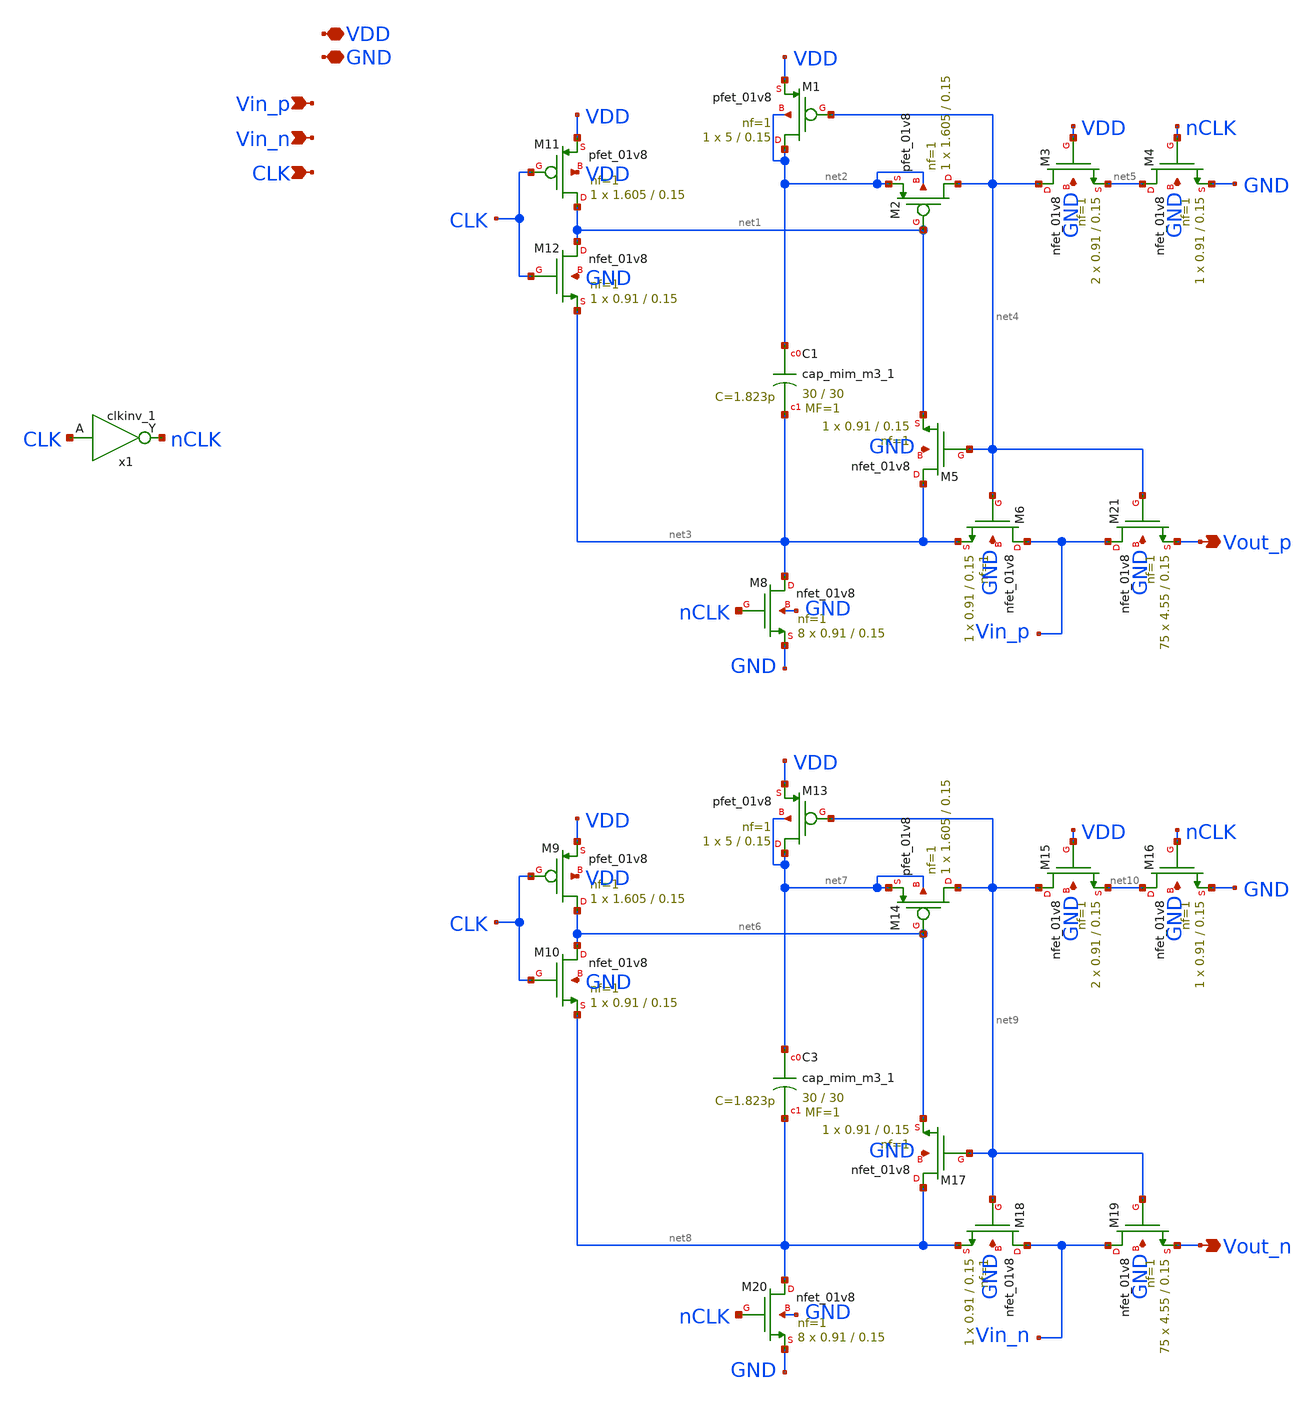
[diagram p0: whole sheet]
** sch_path: xschem/bootstrapped_switch/bsswitch.sch
**.subckt bsswitch Vin_p Vin_n CLK Vout_p Vout_n VDD GND
*.ipin Vin_p
*.ipin Vin_n
*.ipin CLK
*.opin Vout_p
*.opin Vout_n
*.iopin VDD
*.iopin GND
XM11 net1 CLK VDD VDD sky130_fd_pr__pfet_01v8 L=0.15 W=1.605 nf=1 ad='int((nf+1)/2) * W/nf * 0.29' as='int((nf+2)/2) * W/nf * 0.29'
+ pd='2*int((nf+1)/2) * (W/nf + 0.29)' ps='2*int((nf+2)/2) * (W/nf + 0.29)' nrd='0.29 / W' nrs='0.29 / W'
+ sa=0 sb=0 sd=0 mult=1 m=1
XM12 net1 CLK net3 GND sky130_fd_pr__nfet_01v8 L=0.15 W=0.91 nf=1 ad='int((nf+1)/2) * W/nf * 0.29' as='int((nf+2)/2) * W/nf * 0.29'
+ pd='2*int((nf+1)/2) * (W/nf + 0.29)' ps='2*int((nf+2)/2) * (W/nf + 0.29)' nrd='0.29 / W' nrs='0.29 / W'
+ sa=0 sb=0 sd=0 mult=1 m=1
XM1 net2 net4 VDD net2 sky130_fd_pr__pfet_01v8 L=0.15 W=5 nf=1 ad='int((nf+1)/2) * W/nf * 0.29' as='int((nf+2)/2) * W/nf * 0.29'
+ pd='2*int((nf+1)/2) * (W/nf + 0.29)' ps='2*int((nf+2)/2) * (W/nf + 0.29)' nrd='0.29 / W' nrs='0.29 / W'
+ sa=0 sb=0 sd=0 mult=1 m=1
XM2 net4 net1 net2 net2 sky130_fd_pr__pfet_01v8 L=0.15 W=1.605 nf=1 ad='int((nf+1)/2) * W/nf * 0.29'
+ as='int((nf+2)/2) * W/nf * 0.29' pd='2*int((nf+1)/2) * (W/nf + 0.29)' ps='2*int((nf+2)/2) * (W/nf + 0.29)'
+ nrd='0.29 / W' nrs='0.29 / W' sa=0 sb=0 sd=0 mult=1 m=1
XM3 net4 VDD net5 GND sky130_fd_pr__nfet_01v8 L=0.15 W=0.91 nf=1 ad='int((nf+1)/2) * W/nf * 0.29' as='int((nf+2)/2) * W/nf * 0.29'
+ pd='2*int((nf+1)/2) * (W/nf + 0.29)' ps='2*int((nf+2)/2) * (W/nf + 0.29)' nrd='0.29 / W' nrs='0.29 / W'
+ sa=0 sb=0 sd=0 mult=2 m=2
XM4 net5 nCLK GND GND sky130_fd_pr__nfet_01v8 L=0.15 W=0.91 nf=1 ad='int((nf+1)/2) * W/nf * 0.29' as='int((nf+2)/2) * W/nf * 0.29'
+ pd='2*int((nf+1)/2) * (W/nf + 0.29)' ps='2*int((nf+2)/2) * (W/nf + 0.29)' nrd='0.29 / W' nrs='0.29 / W'
+ sa=0 sb=0 sd=0 mult=1 m=1
XM5 net3 net4 net1 GND sky130_fd_pr__nfet_01v8 L=0.15 W=0.91 nf=1 ad='int((nf+1)/2) * W/nf * 0.29' as='int((nf+2)/2) * W/nf * 0.29'
+ pd='2*int((nf+1)/2) * (W/nf + 0.29)' ps='2*int((nf+2)/2) * (W/nf + 0.29)' nrd='0.29 / W' nrs='0.29 / W'
+ sa=0 sb=0 sd=0 mult=1 m=1
XM6 Vin_p net4 net3 GND sky130_fd_pr__nfet_01v8 L=0.15 W=0.91 nf=1 ad='int((nf+1)/2) * W/nf * 0.29' as='int((nf+2)/2) * W/nf * 0.29'
+ pd='2*int((nf+1)/2) * (W/nf + 0.29)' ps='2*int((nf+2)/2) * (W/nf + 0.29)' nrd='0.29 / W' nrs='0.29 / W'
+ sa=0 sb=0 sd=0 mult=1 m=1
XM8 net3 nCLK GND GND sky130_fd_pr__nfet_01v8 L=0.15 W=0.91 nf=1 ad='int((nf+1)/2) * W/nf * 0.29' as='int((nf+2)/2) * W/nf * 0.29'
+ pd='2*int((nf+1)/2) * (W/nf + 0.29)' ps='2*int((nf+2)/2) * (W/nf + 0.29)' nrd='0.29 / W' nrs='0.29 / W'
+ sa=0 sb=0 sd=0 mult=8 m=8
XM9 net6 CLK VDD VDD sky130_fd_pr__pfet_01v8 L=0.15 W=1.605 nf=1 ad='int((nf+1)/2) * W/nf * 0.29' as='int((nf+2)/2) * W/nf * 0.29'
+ pd='2*int((nf+1)/2) * (W/nf + 0.29)' ps='2*int((nf+2)/2) * (W/nf + 0.29)' nrd='0.29 / W' nrs='0.29 / W'
+ sa=0 sb=0 sd=0 mult=1 m=1
XM10 net6 CLK net8 GND sky130_fd_pr__nfet_01v8 L=0.15 W=0.91 nf=1 ad='int((nf+1)/2) * W/nf * 0.29' as='int((nf+2)/2) * W/nf * 0.29'
+ pd='2*int((nf+1)/2) * (W/nf + 0.29)' ps='2*int((nf+2)/2) * (W/nf + 0.29)' nrd='0.29 / W' nrs='0.29 / W'
+ sa=0 sb=0 sd=0 mult=1 m=1
XM13 net7 net9 VDD net7 sky130_fd_pr__pfet_01v8 L=0.15 W=5 nf=1 ad='int((nf+1)/2) * W/nf * 0.29' as='int((nf+2)/2) * W/nf * 0.29'
+ pd='2*int((nf+1)/2) * (W/nf + 0.29)' ps='2*int((nf+2)/2) * (W/nf + 0.29)' nrd='0.29 / W' nrs='0.29 / W'
+ sa=0 sb=0 sd=0 mult=1 m=1
XM14 net9 net6 net7 net7 sky130_fd_pr__pfet_01v8 L=0.15 W=1.605 nf=1 ad='int((nf+1)/2) * W/nf * 0.29'
+ as='int((nf+2)/2) * W/nf * 0.29' pd='2*int((nf+1)/2) * (W/nf + 0.29)' ps='2*int((nf+2)/2) * (W/nf + 0.29)'
+ nrd='0.29 / W' nrs='0.29 / W' sa=0 sb=0 sd=0 mult=1 m=1
XM15 net9 VDD net10 GND sky130_fd_pr__nfet_01v8 L=0.15 W=0.91 nf=1 ad='int((nf+1)/2) * W/nf * 0.29' as='int((nf+2)/2) * W/nf * 0.29'
+ pd='2*int((nf+1)/2) * (W/nf + 0.29)' ps='2*int((nf+2)/2) * (W/nf + 0.29)' nrd='0.29 / W' nrs='0.29 / W'
+ sa=0 sb=0 sd=0 mult=2 m=2
XM16 net10 nCLK GND GND sky130_fd_pr__nfet_01v8 L=0.15 W=0.91 nf=1 ad='int((nf+1)/2) * W/nf * 0.29' as='int((nf+2)/2) * W/nf * 0.29'
+ pd='2*int((nf+1)/2) * (W/nf + 0.29)' ps='2*int((nf+2)/2) * (W/nf + 0.29)' nrd='0.29 / W' nrs='0.29 / W'
+ sa=0 sb=0 sd=0 mult=1 m=1
XM17 net8 net9 net6 GND sky130_fd_pr__nfet_01v8 L=0.15 W=0.91 nf=1 ad='int((nf+1)/2) * W/nf * 0.29' as='int((nf+2)/2) * W/nf * 0.29'
+ pd='2*int((nf+1)/2) * (W/nf + 0.29)' ps='2*int((nf+2)/2) * (W/nf + 0.29)' nrd='0.29 / W' nrs='0.29 / W'
+ sa=0 sb=0 sd=0 mult=1 m=1
XM18 Vin_n net9 net8 GND sky130_fd_pr__nfet_01v8 L=0.15 W=0.91 nf=1 ad='int((nf+1)/2) * W/nf * 0.29'
+ as='int((nf+2)/2) * W/nf * 0.29' pd='2*int((nf+1)/2) * (W/nf + 0.29)' ps='2*int((nf+2)/2) * (W/nf + 0.29)'
+ nrd='0.29 / W' nrs='0.29 / W' sa=0 sb=0 sd=0 mult=1 m=1
XM20 net8 nCLK GND GND sky130_fd_pr__nfet_01v8 L=0.15 W=0.91 nf=1 ad='int((nf+1)/2) * W/nf * 0.29' as='int((nf+2)/2) * W/nf * 0.29'
+ pd='2*int((nf+1)/2) * (W/nf + 0.29)' ps='2*int((nf+2)/2) * (W/nf + 0.29)' nrd='0.29 / W' nrs='0.29 / W'
+ sa=0 sb=0 sd=0 mult=8 m=8
XC3 net7 net8 sky130_fd_pr__cap_mim_m3_1 W=30 L=30 MF=1 m=1
XM19 Vin_n net9 Vout_n GND sky130_fd_pr__nfet_01v8 L=0.15 W=4.55 nf=1 ad='int((nf+1)/2) * W/nf * 0.29'
+ as='int((nf+2)/2) * W/nf * 0.29' pd='2*int((nf+1)/2) * (W/nf + 0.29)' ps='2*int((nf+2)/2) * (W/nf + 0.29)'
+ nrd='0.29 / W' nrs='0.29 / W' sa=0 sb=0 sd=0 mult=75 m=75
XM21 Vin_p net4 Vout_p GND sky130_fd_pr__nfet_01v8 L=0.15 W=4.55 nf=1 ad='int((nf+1)/2) * W/nf * 0.29'
+ as='int((nf+2)/2) * W/nf * 0.29' pd='2*int((nf+1)/2) * (W/nf + 0.29)' ps='2*int((nf+2)/2) * (W/nf + 0.29)'
+ nrd='0.29 / W' nrs='0.29 / W' sa=0 sb=0 sd=0 mult=75 m=75
XC1 net2 net3 sky130_fd_pr__cap_mim_m3_1 W=30 L=30 MF=1 m=1
x1 CLK GND GND VDD VDD nCLK sky130_fd_sc_hd__clkinv_1
**.ends
.end
